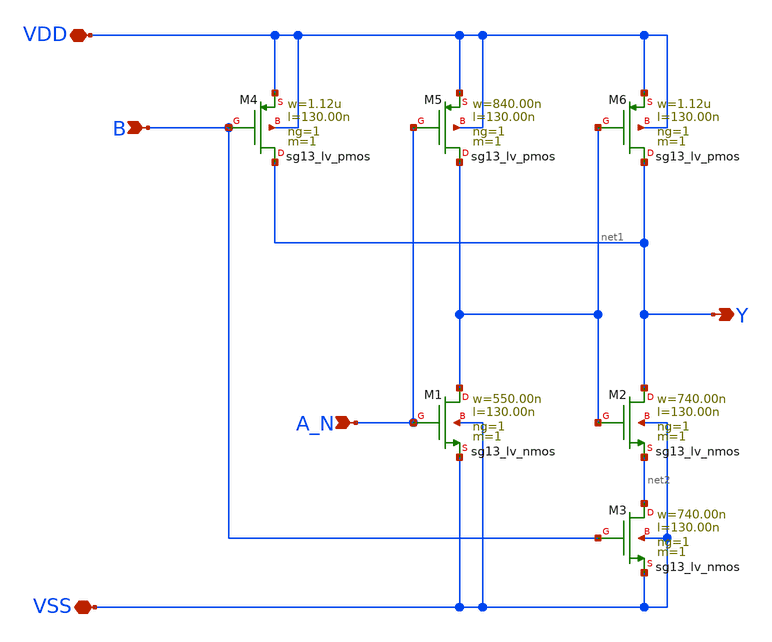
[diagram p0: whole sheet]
** sch_path: ihp-sg13g2/libs.tech/xschem/sg13g2_stdcells/sg13g2_nand2b_1.sch
* Copyright 2023 IHP PDK Authors
* Licensed under the Apache License, Version 2.0 (the "License");
* you may not use this file except in compliance with the License.
* You may obtain a copy of the License at
* https://www.apache.org/licenses/LICENSE-2.0
* Unless required by applicable law or agreed to in writing, software
* distributed under the License is distributed on an "AS IS" BASIS,
* WITHOUT WARRANTIES OR CONDITIONS OF ANY KIND, either express or implied.
* See the License for the specific language governing permissions and
* limitations under the License.
**.subckt sg13g2_nand2b_1 Y B A_N VDD VSS
*.opin Y
*.ipin B
*.ipin A_N
*.iopin VDD
*.iopin VSS
XM1 net1 A_N VSS VSS sg13_lv_nmos w=550.00n l=130.00n ng=1 m=1 mm_ok=1
XM2 Y net1 net2 VSS sg13_lv_nmos w=740.00n l=130.00n ng=1 m=1 mm_ok=1
XM3 net2 B VSS VSS sg13_lv_nmos w=740.00n l=130.00n ng=1 m=1 mm_ok=1
XM4 Y B VDD VDD sg13_lv_pmos w=1.12u l=130.00n ng=1 m=1 mm_ok=1
XM5 net1 A_N VDD VDD sg13_lv_pmos w=840.00n l=130.00n ng=1 m=1 mm_ok=1
XM6 Y net1 VDD VDD sg13_lv_pmos w=1.12u l=130.00n ng=1 m=1 mm_ok=1
**.ends
.end
